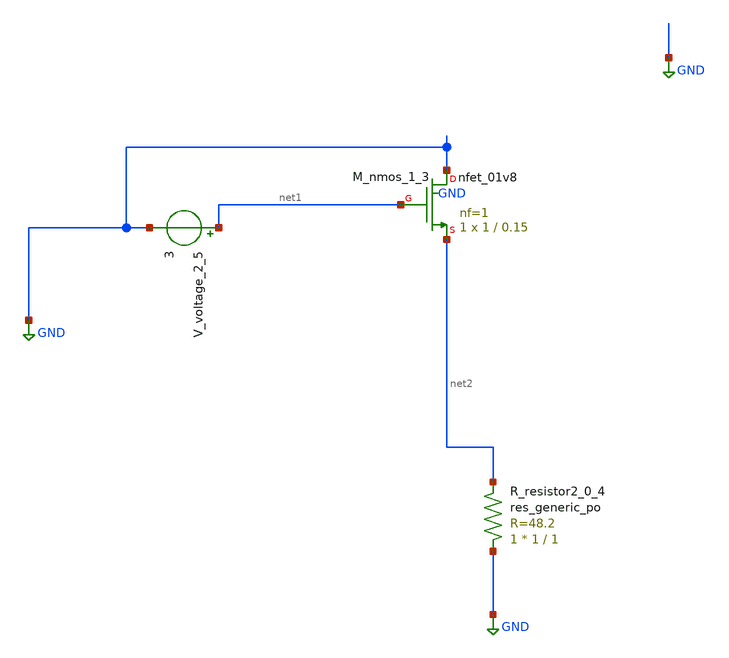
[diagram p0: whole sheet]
** sch_path: schematics/AMSNet/453.sch
**.subckt 453
XM_nmos_1_3 GND net1 net2 GND sky130_fd_pr__nfet_01v8 L=0.15 W=1 nf=1 ad='int((1 + 1)/2) * 1 / 1 * 0.29'
+ as='int((1 + 2)/2) * 1 / 1 * 0.29' pd='2*int((1 + 1)/2) * (1 / 1 + 0.29)' ps='2*int((1 + 2)/2) * (1 / 1 + 0.29)'
+ nrd='0.29 / 1 ' nrs='0.29 / 1 ' sa=0 sb=0 sd=0 mult=1 m=1
XR_resistor2_0_4 GND net2 sky130_fd_pr__res_generic_po W=1 L=1 m=1
V_voltage_2_5 net1 GND 3
**.ends
.GLOBAL GND
.end
